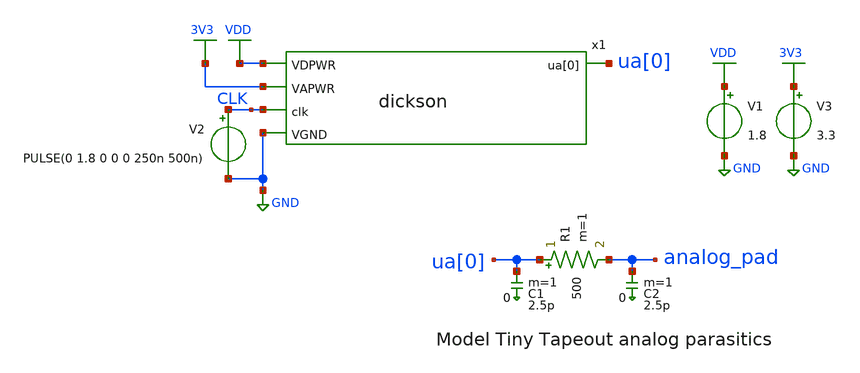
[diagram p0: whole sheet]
** sch_path: tt_um_urish_charge_pump/xschem/testbench.sch
**.subckt testbench
x1 VDD 3V3 CLK ua[0] GND dickson
V1 VDD GND 1.8
V2 CLK GND PULSE(0 1.8 0 0 0 250n 500n)
R1 ua[0] analog_pad 500 m=1
C1 ua[0] 0 2.5p m=1
C2 analog_pad 0 2.5p m=1
V3 3V3 GND 3.3
**** begin user architecture code

** opencircuitdesign pdks install
.lib $::SKYWATER_MODELS/sky130.lib.spice tt





.tran 10n 100u
.save all

.control
run
write testbench.raw
.endc


**** end user architecture code
**.ends
.GLOBAL GND
.GLOBAL VDD
.GLOBAL 3V3
.end
